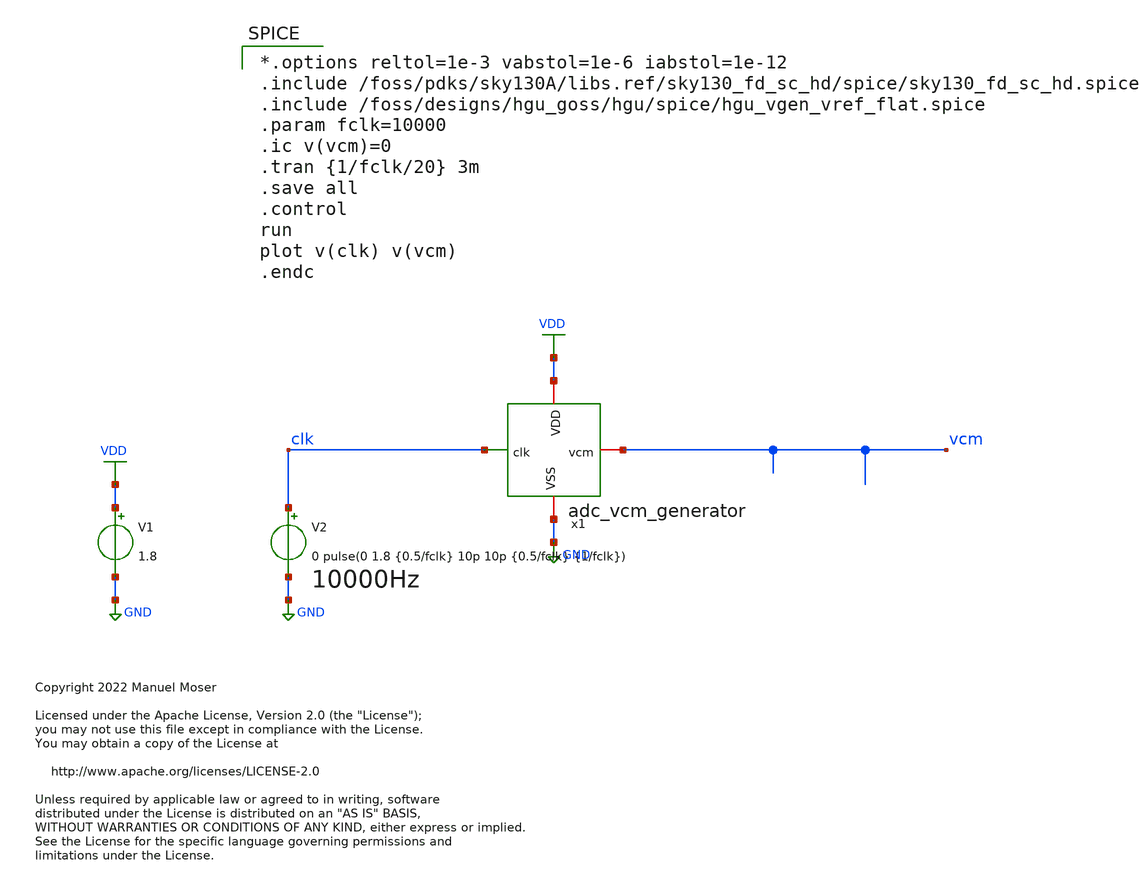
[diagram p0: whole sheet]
** sch_path: tb/tb_hgu_vgen_vref.sch
* Copyright 2022 Manuel Moser
* Licensed under the Apache License, Version 2.0 (the "License");
**.subckt tb_hgu_vgen_vref
V1 VDD GND 1.8
V2 clk GND 0 pulse(0 1.8 {0.5/fclk} 10p 10p {0.5/fclk} {1/fclk})
x1 VDD vcm clk GND adc_vcm_generator
**** begin user architecture code

*.options reltol=1e-3 vabstol=1e-6 iabstol=1e-12
.include /foss/pdks/sky130A/libs.ref/sky130_fd_sc_hd/spice/sky130_fd_sc_hd.spice
.include /foss/designs/hgu_goss/hgu/spice/hgu_vgen_vref_flat.spice
.param fclk=10000
.ic v(vcm)=0
.tran {1/fclk/20} 3m
.save all
.control
run
plot v(clk) v(vcm)
.endc



** opencircuitdesign pdks install
.lib $::SKYWATER_MODELS/sky130.lib.spice tt


**** end user architecture code
**.ends
.GLOBAL GND
.GLOBAL VDD
.end
